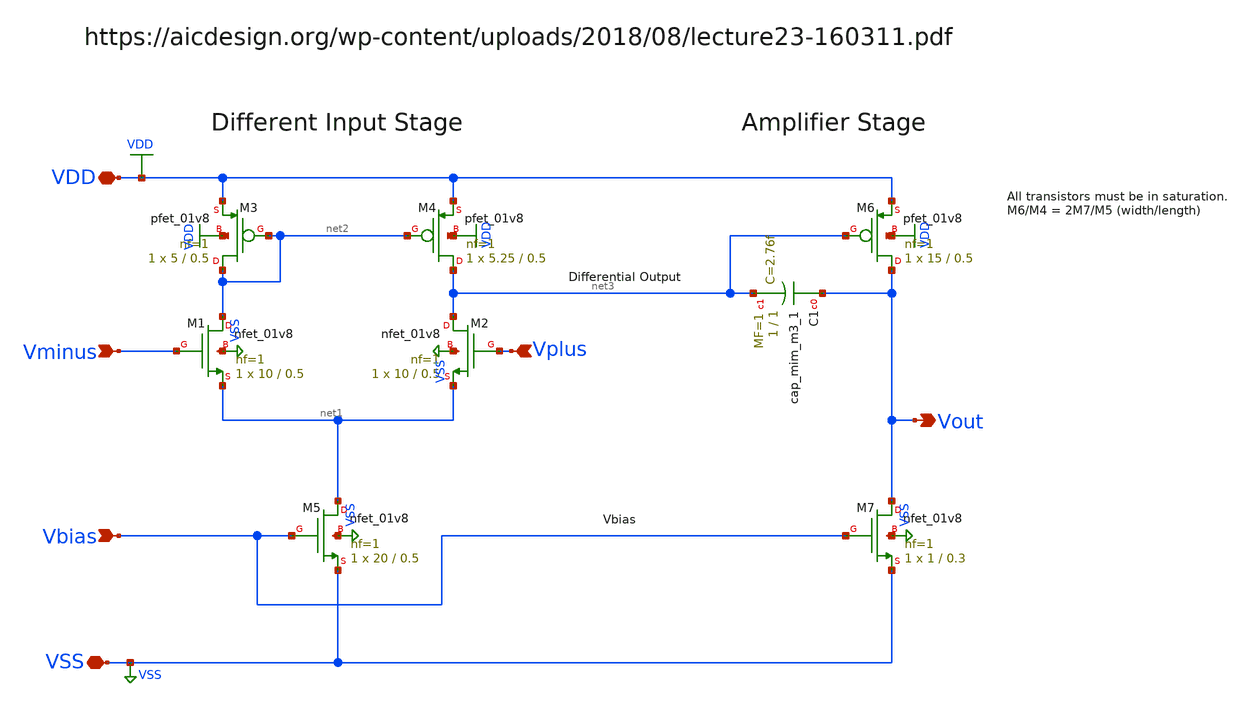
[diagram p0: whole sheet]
** sch_path: examples/template/temp_schemsym_204802182e594a91b3edb52b763f5c80.sch
**.subckt temp_schemsym_204802182e594a91b3edb52b763f5c80 Vplus Vminus VDD VSS Vbias Vout
*.ipin Vplus
*.ipin Vminus
*.iopin VDD
*.iopin VSS
*.ipin Vbias
*.opin Vout
XM1 net2 Vminus net1 VSS sky130_fd_pr__nfet_01v8 L=0.5 W=10 nf=1 ad='int((nf+1)/2) * W/nf * 0.29' as='int((nf+2)/2) * W/nf * 0.29'
+ pd='2*int((nf+1)/2) * (W/nf + 0.29)' ps='2*int((nf+2)/2) * (W/nf + 0.29)' nrd='0.29 / W' nrs='0.29 / W'
+ sa=0 sb=0 sd=0 mult=1 m=1
XM2 net3 Vplus net1 VSS sky130_fd_pr__nfet_01v8 L=0.5 W=10 nf=1 ad='int((nf+1)/2) * W/nf * 0.29' as='int((nf+2)/2) * W/nf * 0.29'
+ pd='2*int((nf+1)/2) * (W/nf + 0.29)' ps='2*int((nf+2)/2) * (W/nf + 0.29)' nrd='0.29 / W' nrs='0.29 / W'
+ sa=0 sb=0 sd=0 mult=1 m=1
XM3 net2 net2 VDD VDD sky130_fd_pr__pfet_01v8 L=0.5 W=5 nf=1 ad='int((nf+1)/2) * W/nf * 0.29' as='int((nf+2)/2) * W/nf * 0.29'
+ pd='2*int((nf+1)/2) * (W/nf + 0.29)' ps='2*int((nf+2)/2) * (W/nf + 0.29)' nrd='0.29 / W' nrs='0.29 / W'
+ sa=0 sb=0 sd=0 mult=1 m=1
XM4 net3 net2 VDD VDD sky130_fd_pr__pfet_01v8 L=0.5 W=5.25 nf=1 ad='int((nf+1)/2) * W/nf * 0.29' as='int((nf+2)/2) * W/nf * 0.29'
+ pd='2*int((nf+1)/2) * (W/nf + 0.29)' ps='2*int((nf+2)/2) * (W/nf + 0.29)' nrd='0.29 / W' nrs='0.29 / W'
+ sa=0 sb=0 sd=0 mult=1 m=1
XM5 net1 Vbias VSS VSS sky130_fd_pr__nfet_01v8 L=0.5 W=20 nf=1 ad='int((nf+1)/2) * W/nf * 0.29' as='int((nf+2)/2) * W/nf * 0.29'
+ pd='2*int((nf+1)/2) * (W/nf + 0.29)' ps='2*int((nf+2)/2) * (W/nf + 0.29)' nrd='0.29 / W' nrs='0.29 / W'
+ sa=0 sb=0 sd=0 mult=1 m=1
XM6 Vout net3 VDD VDD sky130_fd_pr__pfet_01v8 L=0.5 W=15 nf=1 ad='int((nf+1)/2) * W/nf * 0.29' as='int((nf+2)/2) * W/nf * 0.29'
+ pd='2*int((nf+1)/2) * (W/nf + 0.29)' ps='2*int((nf+2)/2) * (W/nf + 0.29)' nrd='0.29 / W' nrs='0.29 / W'
+ sa=0 sb=0 sd=0 mult=1 m=1
XC1 Vout net3 sky130_fd_pr__cap_mim_m3_1 W=1 L=1 MF=1 m=1
XM7 Vout Vbias VSS VSS sky130_fd_pr__nfet_01v8 L=0.3 W=1 nf=1 ad='int((nf+1)/2) * W/nf * 0.29' as='int((nf+2)/2) * W/nf * 0.29'
+ pd='2*int((nf+1)/2) * (W/nf + 0.29)' ps='2*int((nf+2)/2) * (W/nf + 0.29)' nrd='0.29 / W' nrs='0.29 / W'
+ sa=0 sb=0 sd=0 mult=1 m=1
**.ends
.GLOBAL VDD
.GLOBAL VSS
.end
